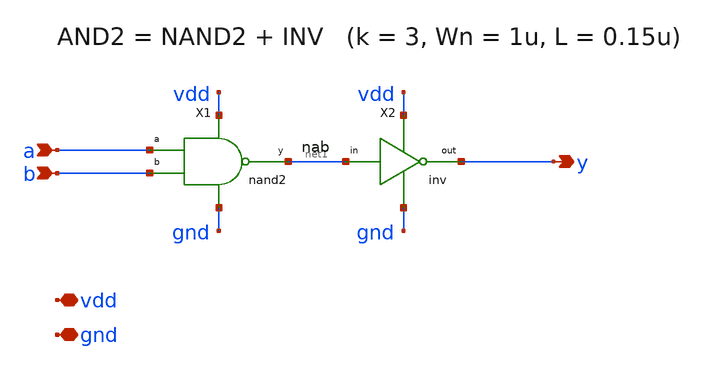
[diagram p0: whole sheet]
** sch_path: proj/xschem/and2.sch
**.subckt and2 a b y vdd gnd
*.ipin a
*.ipin b
*.opin y
*.iopin vdd
*.iopin gnd
X1 a b net1 vdd gnd nand2
X2 net1 y vdd gnd inv
**.ends

* expanding   symbol:  nand2.sym # of pins=5
** sym_path: proj/xschem/nand2.sym
** sch_path: proj/xschem/nand2.sch
.subckt nand2 a b y vdd gnd
*.ipin a
*.ipin b
*.opin y
*.iopin vdd
*.iopin gnd
XMPA y a vdd vdd sky130_fd_pr__pfet_01v8 L=0.15 W=3 nf=1 ad='int((1 + 1)/2) * 3 / 1 * 0.29' as='int((1 + 2)/2) * 3 / 1 * 0.29'
+ pd='2*int((1 + 1)/2) * (3 / 1 + 0.29)' ps='2*int((1 + 2)/2) * (3 / 1 + 0.29)' nrd='0.29 / 3 ' nrs='0.29 / 3 '
+ sa=0 sb=0 sd=0 mult=1 m=1
XMPB y b vdd vdd sky130_fd_pr__pfet_01v8 L=0.15 W=3 nf=1 ad='int((1 + 1)/2) * 3 / 1 * 0.29' as='int((1 + 2)/2) * 3 / 1 * 0.29'
+ pd='2*int((1 + 1)/2) * (3 / 1 + 0.29)' ps='2*int((1 + 2)/2) * (3 / 1 + 0.29)' nrd='0.29 / 3 ' nrs='0.29 / 3 '
+ sa=0 sb=0 sd=0 mult=1 m=1
XMNA y a net1 gnd sky130_fd_pr__nfet_01v8 L=0.15 W=2 nf=1 ad='int((nf+1)/2) * W/nf * 0.29' as='int((nf+2)/2) * W/nf * 0.29'
+ pd='2*int((nf+1)/2) * (W/nf + 0.29)' ps='2*int((nf+2)/2) * (W/nf + 0.29)' nrd='0.29 / W' nrs='0.29 / W'
+ sa=0 sb=0 sd=0 mult=1 m=1
XMNB net1 b gnd gnd sky130_fd_pr__nfet_01v8 L=0.15 W=2 nf=1 ad='int((nf+1)/2) * W/nf * 0.29' as='int((nf+2)/2) * W/nf * 0.29'
+ pd='2*int((nf+1)/2) * (W/nf + 0.29)' ps='2*int((nf+2)/2) * (W/nf + 0.29)' nrd='0.29 / W' nrs='0.29 / W'
+ sa=0 sb=0 sd=0 mult=1 m=1
.ends


* expanding   symbol:  inv.sym # of pins=4
** sym_path: proj/xschem/inv.sym
** sch_path: proj/xschem/inv.sch
.subckt inv in out vdd gnd
*.ipin in
*.opin out
*.iopin vdd
*.iopin gnd
XMP out in vdd vdd sky130_fd_pr__pfet_01v8 L=0.15 W=3 nf=1 ad='int((1 + 1)/2) * 3 / 1 * 0.29' as='int((1 + 2)/2) * 3 / 1 * 0.29'
+ pd='2*int((1 + 1)/2) * (3 / 1 + 0.29)' ps='2*int((1 + 2)/2) * (3 / 1 + 0.29)' nrd='0.29 / 3 ' nrs='0.29 / 3 '
+ sa=0 sb=0 sd=0 mult=1 m=1
XMN out in gnd gnd sky130_fd_pr__nfet_01v8 L=0.15 W=1 nf=1 ad='int((nf+1)/2) * W/nf * 0.29' as='int((nf+2)/2) * W/nf * 0.29'
+ pd='2*int((nf+1)/2) * (W/nf + 0.29)' ps='2*int((nf+2)/2) * (W/nf + 0.29)' nrd='0.29 / W' nrs='0.29 / W'
+ sa=0 sb=0 sd=0 mult=1 m=1
.ends

.end
